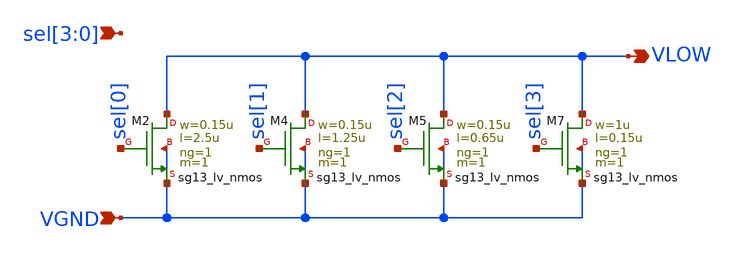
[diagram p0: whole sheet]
** sch_path: xschem/nmosbank.sch
**.subckt nmosbank VGND VLOW sel[3],sel[2],sel[1],sel[0]
*.ipin VGND
*.opin VLOW
*.ipin sel[3],sel[2],sel[1],sel[0]
XM2 VLOW sel[0] VGND VGND sg13_lv_nmos w=0.15u l=2.5u ng=1 m=1 mm_ok=1
XM4 VLOW sel[1] VGND VGND sg13_lv_nmos w=0.15u l=1.25u ng=1 m=1 mm_ok=1
XM5 VLOW sel[2] VGND VGND sg13_lv_nmos w=0.15u l=0.65u ng=1 m=1 mm_ok=1
XM7 VLOW sel[3] VGND VGND sg13_lv_nmos w=1u l=0.15u ng=1 m=1 mm_ok=1
**.ends
.end
